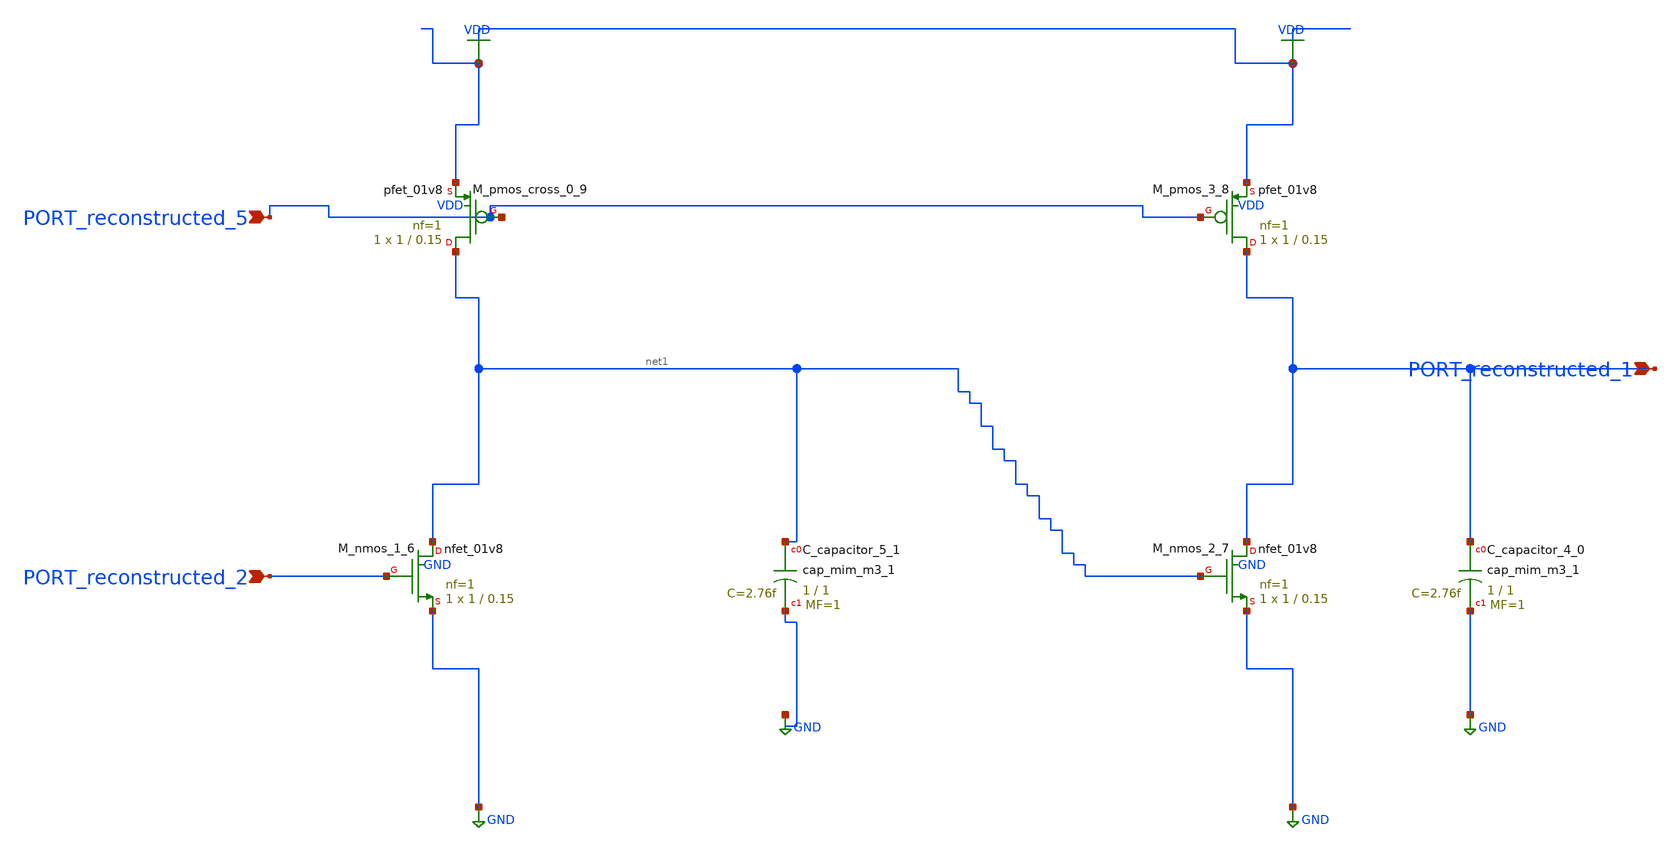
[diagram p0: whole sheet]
** sch_path: schematics/AMSNet/397.sch
**.subckt 397 PORT_reconstructed_1 PORT_reconstructed_2 PORT_reconstructed_5
*.ipin PORT_reconstructed_1
*.ipin PORT_reconstructed_2
*.ipin PORT_reconstructed_5
XC_capacitor_4_0 PORT_reconstructed_1 GND sky130_fd_pr__cap_mim_m3_1 W=1 L=1 MF=1 m=1
XC_capacitor_5_1 net1 GND sky130_fd_pr__cap_mim_m3_1 W=1 L=1 MF=1 m=1
XM_nmos_1_6 net1 PORT_reconstructed_2 GND GND sky130_fd_pr__nfet_01v8 L=0.15 W=1 nf=1 ad='int((1 + 1)/2) * 1 / 1 * 0.29'
+ as='int((1 + 2)/2) * 1 / 1 * 0.29' pd='2*int((1 + 1)/2) * (1 / 1 + 0.29)' ps='2*int((1 + 2)/2) * (1 / 1 + 0.29)'
+ nrd='0.29 / 1 ' nrs='0.29 / 1 ' sa=0 sb=0 sd=0 mult=1 m=1
XM_nmos_2_7 PORT_reconstructed_1 net1 GND GND sky130_fd_pr__nfet_01v8 L=0.15 W=1 nf=1 ad='int((1 + 1)/2) * 1 / 1 * 0.29'
+ as='int((1 + 2)/2) * 1 / 1 * 0.29' pd='2*int((1 + 1)/2) * (1 / 1 + 0.29)' ps='2*int((1 + 2)/2) * (1 / 1 + 0.29)'
+ nrd='0.29 / 1 ' nrs='0.29 / 1 ' sa=0 sb=0 sd=0 mult=1 m=1
XM_pmos_3_8 PORT_reconstructed_1 PORT_reconstructed_5 VDD VDD sky130_fd_pr__pfet_01v8 L=0.15 W=1 nf=1
+ ad='int((1 + 1)/2) * 1 / 1 * 0.29' as='int((1 + 2)/2) * 1 / 1 * 0.29' pd='2*int((1 + 1)/2) * (1 / 1 + 0.29)'
+ ps='2*int((1 + 2)/2) * (1 / 1 + 0.29)' nrd='0.29 / 1 ' nrs='0.29 / 1 ' sa=0 sb=0 sd=0 mult=1 m=1
XM_pmos_cross_0_9 net1 PORT_reconstructed_5 VDD VDD sky130_fd_pr__pfet_01v8 L=0.15 W=1 nf=1 ad='int((1 + 1)/2) * 1 / 1 * 0.29'
+ as='int((1 + 2)/2) * 1 / 1 * 0.29' pd='2*int((1 + 1)/2) * (1 / 1 + 0.29)' ps='2*int((1 + 2)/2) * (1 / 1 + 0.29)'
+ nrd='0.29 / 1 ' nrs='0.29 / 1 ' sa=0 sb=0 sd=0 mult=1 m=1
**.ends
.GLOBAL GND
.GLOBAL VDD
.end
